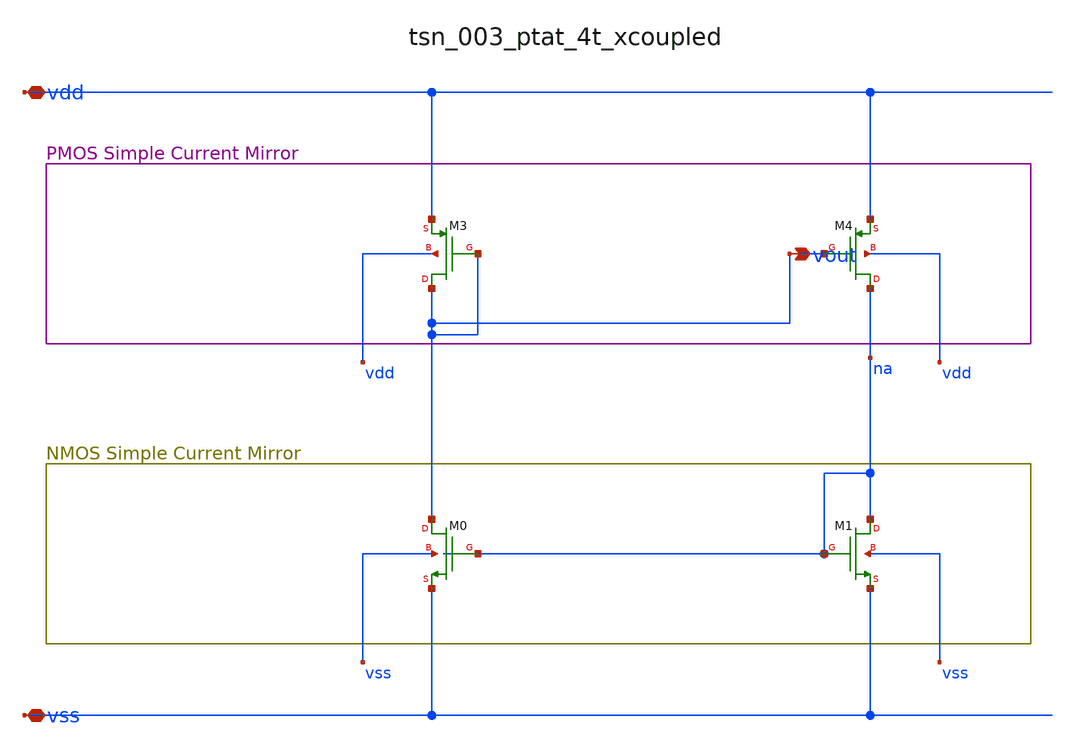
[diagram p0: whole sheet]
** sch_path: analog-db/raw/tsn_003_ptat_4t_xcoupled/tsn_003_ptat_4t_xcoupled_annotated.sch
**.subckt tsn_003_ptat_4t_xcoupled_annotated vdd vss vout
*.iopin vdd
*.iopin vss
*.opin vout
XM0 vout na vss vss sg13_lv_nmos w=x_dut_xm0_w l=x_dut_xm0_l ng=1 m=x_dut_xm0_m
XM1 na na vss vss sg13_lv_nmos w=x_dut_xm1_w l=x_dut_xm1_l ng=1 m=x_dut_xm1_m
XM3 vout vout vdd vdd sg13_lv_pmos w=x_dut_xm3_w l=x_dut_xm3_l ng=1 m=x_dut_xm3_m
XM4 na vout vdd vdd sg13_lv_pmos w=x_dut_xm4_w l=x_dut_xm4_l ng=1 m=x_dut_xm4_m
**.ends
.end
